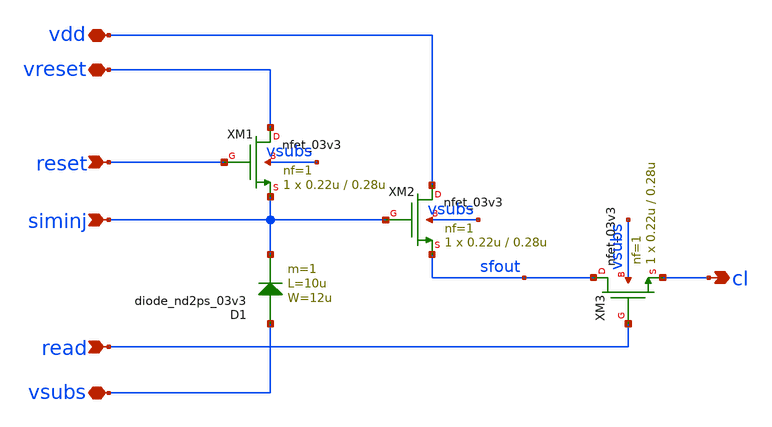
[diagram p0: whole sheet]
** sch_path: xschem/ip_pixel_nw2ps.sch
**.subckt ip_pixel_nw2ps vdd vsubs siminj reset read vreset cl
*.iopin vdd
*.iopin vsubs
*.ipin siminj
*.ipin reset
*.ipin read
*.iopin vreset
*.opin cl
XM1 vreset reset siminj vsubs nfet_03v3 L=0.28u W=0.22u nf=1 ad='int((nf+1)/2) * W/nf * 0.18u' as='int((nf+2)/2) * W/nf * 0.18u'
+ pd='2*int((nf+1)/2) * (W/nf + 0.18u)' ps='2*int((nf+2)/2) * (W/nf + 0.18u)' nrd='0.18u / W' nrs='0.18u / W'
+ sa=0 sb=0 sd=0 m=1
XM2 vdd siminj sfout vsubs nfet_03v3 L=0.28u W=0.22u nf=1 ad='int((nf+1)/2) * W/nf * 0.18u' as='int((nf+2)/2) * W/nf * 0.18u'
+ pd='2*int((nf+1)/2) * (W/nf + 0.18u)' ps='2*int((nf+2)/2) * (W/nf + 0.18u)' nrd='0.18u / W' nrs='0.18u / W'
+ sa=0 sb=0 sd=0 m=1
XM3 sfout read cl vsubs nfet_03v3 L=0.28u W=0.22u nf=1 ad='int((nf+1)/2) * W/nf * 0.18u' as='int((nf+2)/2) * W/nf * 0.18u'
+ pd='2*int((nf+1)/2) * (W/nf + 0.18u)' ps='2*int((nf+2)/2) * (W/nf + 0.18u)' nrd='0.18u / W' nrs='0.18u / W'
+ sa=0 sb=0 sd=0 m=1
D1 vsubs siminj diode_nd2ps_03v3 w=12u l=10u area='12u * 10u ' pj='2*12u + 2*10u ' m=1
**.ends
.end
